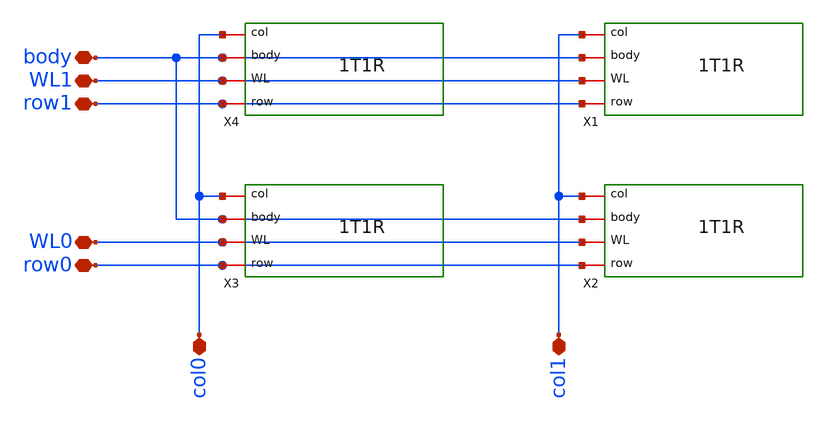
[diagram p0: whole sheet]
** sch_path: xschem/1T1R_2x2.sch
* StefanSchippers/xschem_sky130/sky130_fd_pr/reram.sym:
* Copyright 2021 Stefan Frederik Schippers
* Licensed under the Apache License, Version 2.0 (the "License");
**.subckt 1T1R_2x2 row1 WL1 row0 WL0 body col0 col1
*.iopin row1
*.iopin WL1
*.iopin row0
*.iopin WL0
*.iopin body
*.iopin col0
*.iopin col1
X1 row1 WL1 body col1 1T1R
X2 row0 WL0 body col1 1T1R
X3 row0 WL0 body col0 1T1R
X4 row1 WL1 body col0 1T1R
**.ends

* expanding   symbol:  /Volumes/export/isn/soumil/ReRAM_sky130_files/1T1R.sym # of pins=4
** sym_path: xschem/1T1R.sym
** sch_path: xschem/1T1R.sch
.subckt 1T1R row WL body col
*.iopin WL
*.iopin body
*.iopin row
*.iopin col
XM1 net1 WL col body sky130_fd_pr__nfet_g5v0d10v5 L=0.5 W=1 nf=1 ad='int((nf+1)/2) * W/nf * 0.29' as='int((nf+2)/2) * W/nf * 0.29'
+ pd='2*int((nf+1)/2) * (W/nf + 0.29)' ps='2*int((nf+2)/2) * (W/nf + 0.29)' nrd='0.29 / W' nrs='0.29 / W'
+ sa=0 sb=0 sd=0 mult=1 m=1
XR1 row net1 reram_reram_cell Tfilament_0=3.8e-9
.ends

**** begin user architecture code

.subckt sky130_fd_pr_reram__reram_cell TE BE Tfilament_0=3.3e-9 area_ox=0.1024e-12
N1 TE BE nFilament sky130_fd_pr_reram__reram_model
.ic v(nFilament)={Tfilament_0*1.0e9}
.ends sky130_fd_pr_reram__reram_cell

.model sky130_fd_pr_reram__reram_model sky130_fd_pr_reram__reram_module  area_ox = 0.1024e-12  Tox =
+ 5.0  Tfilament_max = 4.9  Tfilament_min = 3.3  Eact_generation = 1.501  Eact_recombination  = 1.500
+  I_k1  = 6.140e-5  Tfilament_ref = 4.7249  V_ref = 0.430  velocity_k1 = 150  gamma_k0  = 16.5  gamma_k1
+  = -1.25  Temperature_0 = 300  C_thermal = 3.1825e-16  tau_thermal = 0.23e-9  t_step  = 1.0e-9
+  smoothing = 1e-7  Kclip = 200

.control
pre_osdi $SKYWATER_MODELS/sky130_fd_pr_reram__reram_module.osdi
.endc

**** end user architecture code
.end
